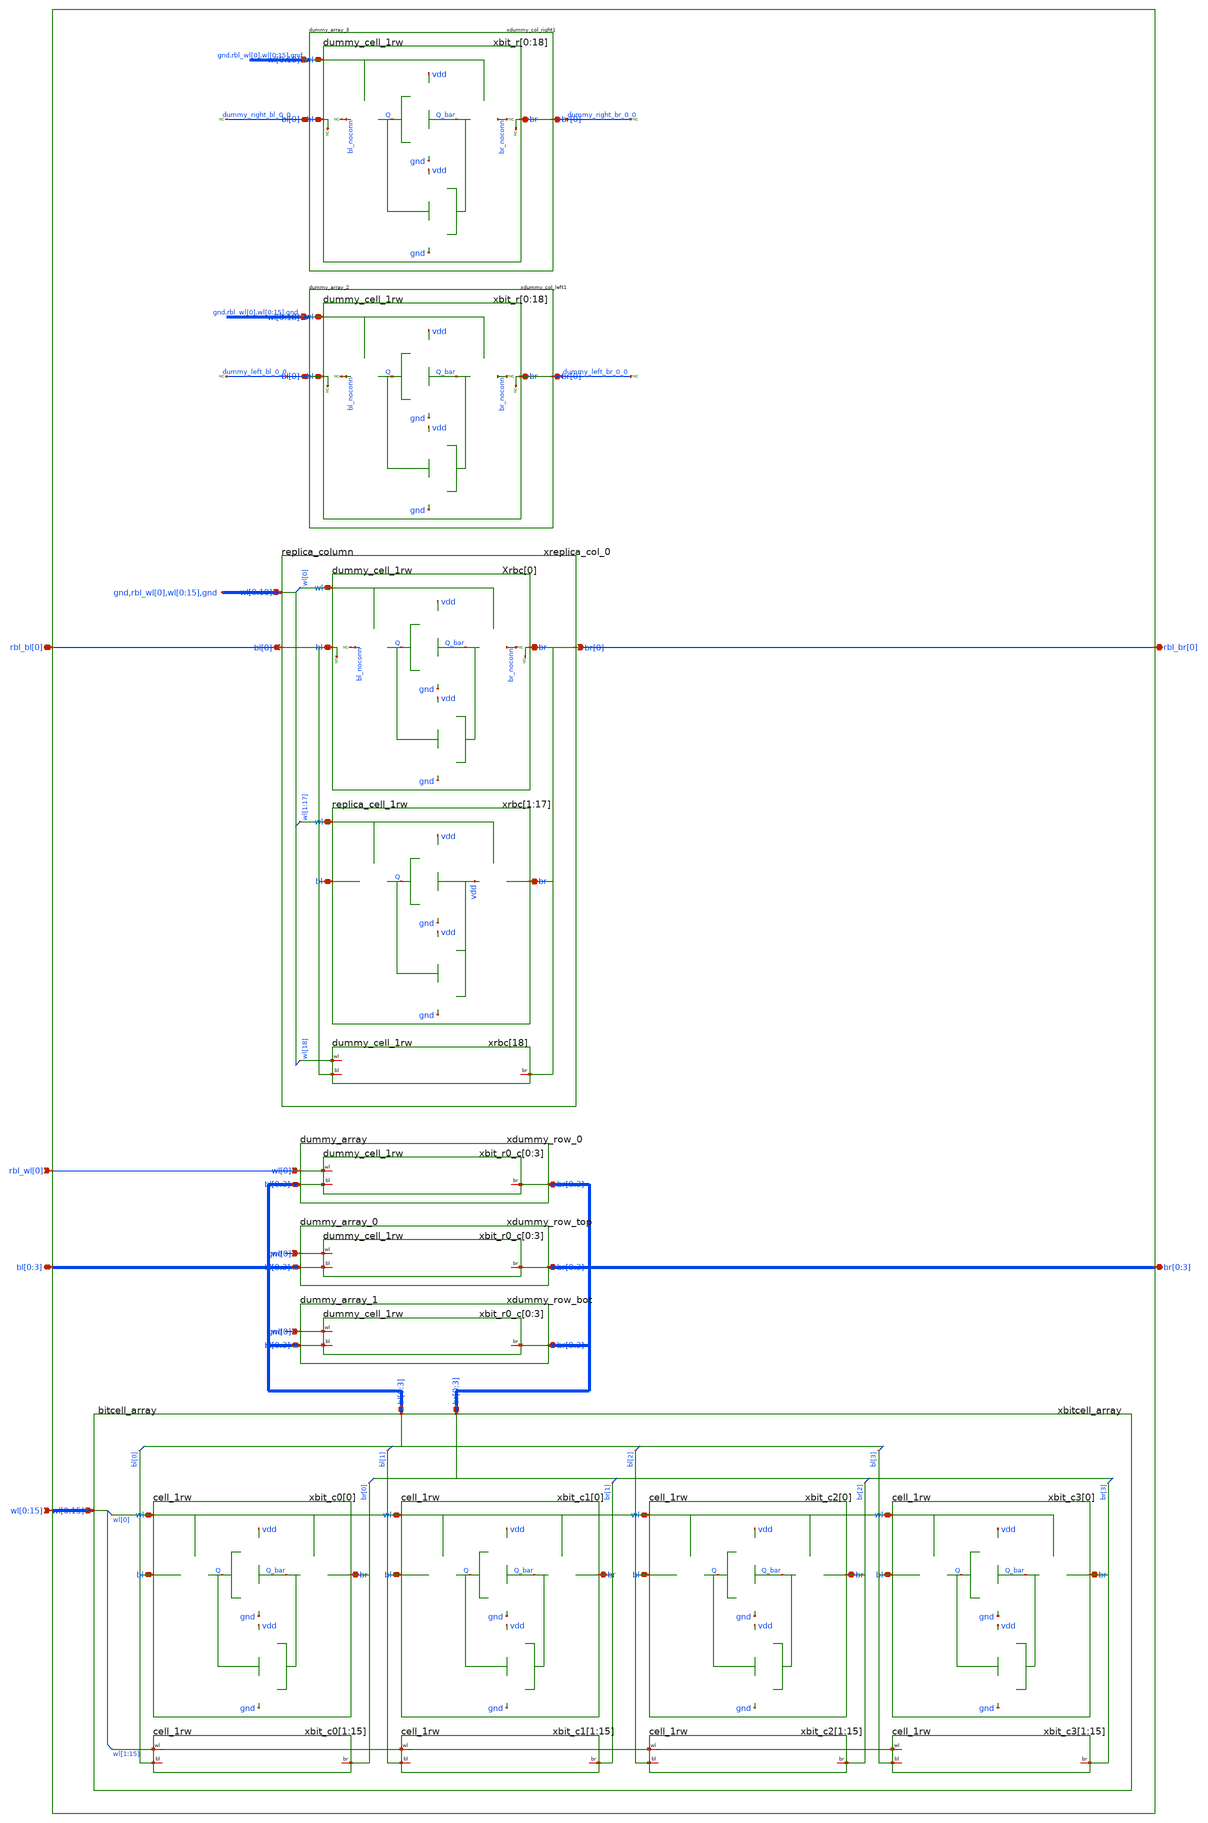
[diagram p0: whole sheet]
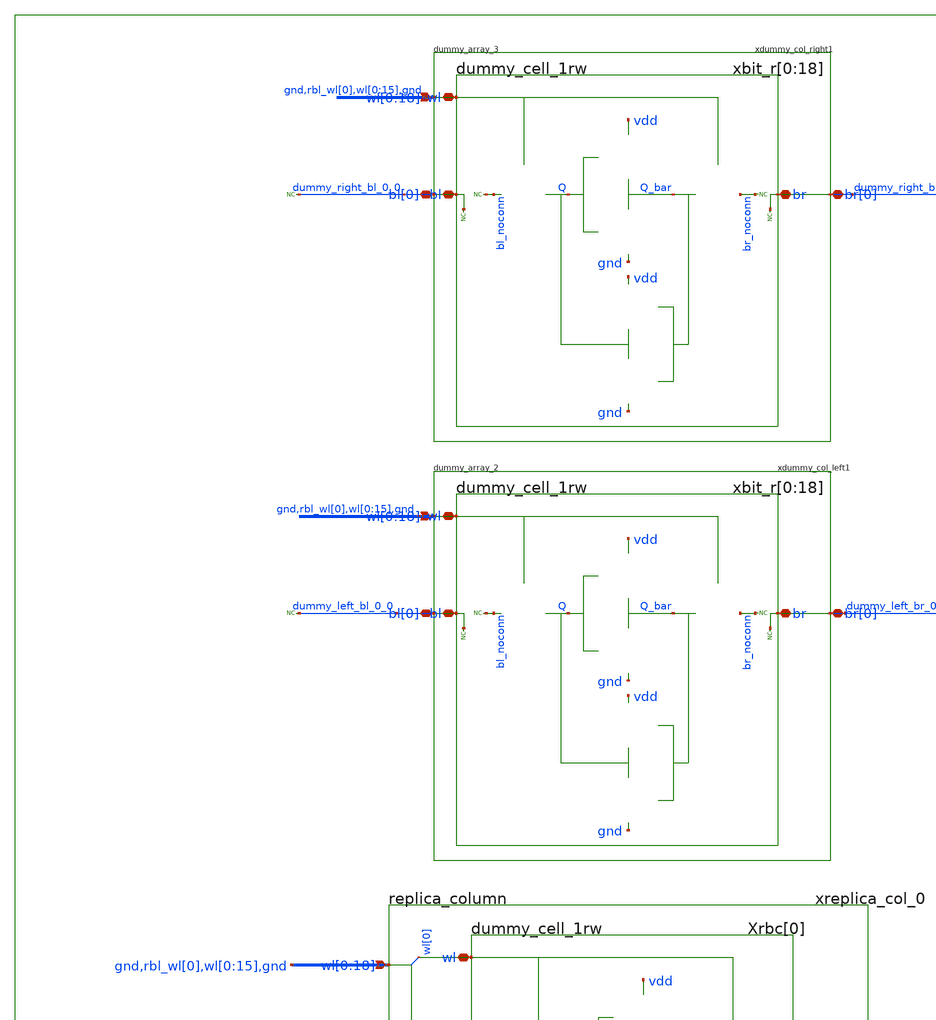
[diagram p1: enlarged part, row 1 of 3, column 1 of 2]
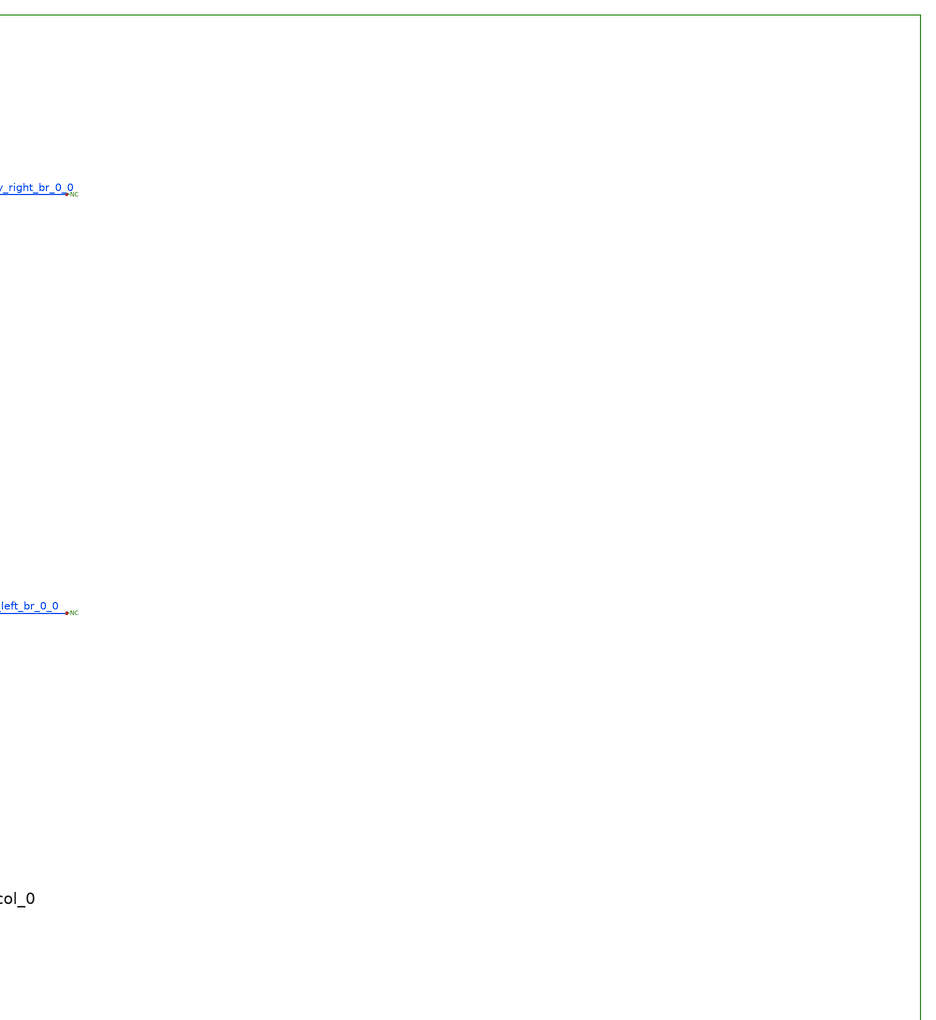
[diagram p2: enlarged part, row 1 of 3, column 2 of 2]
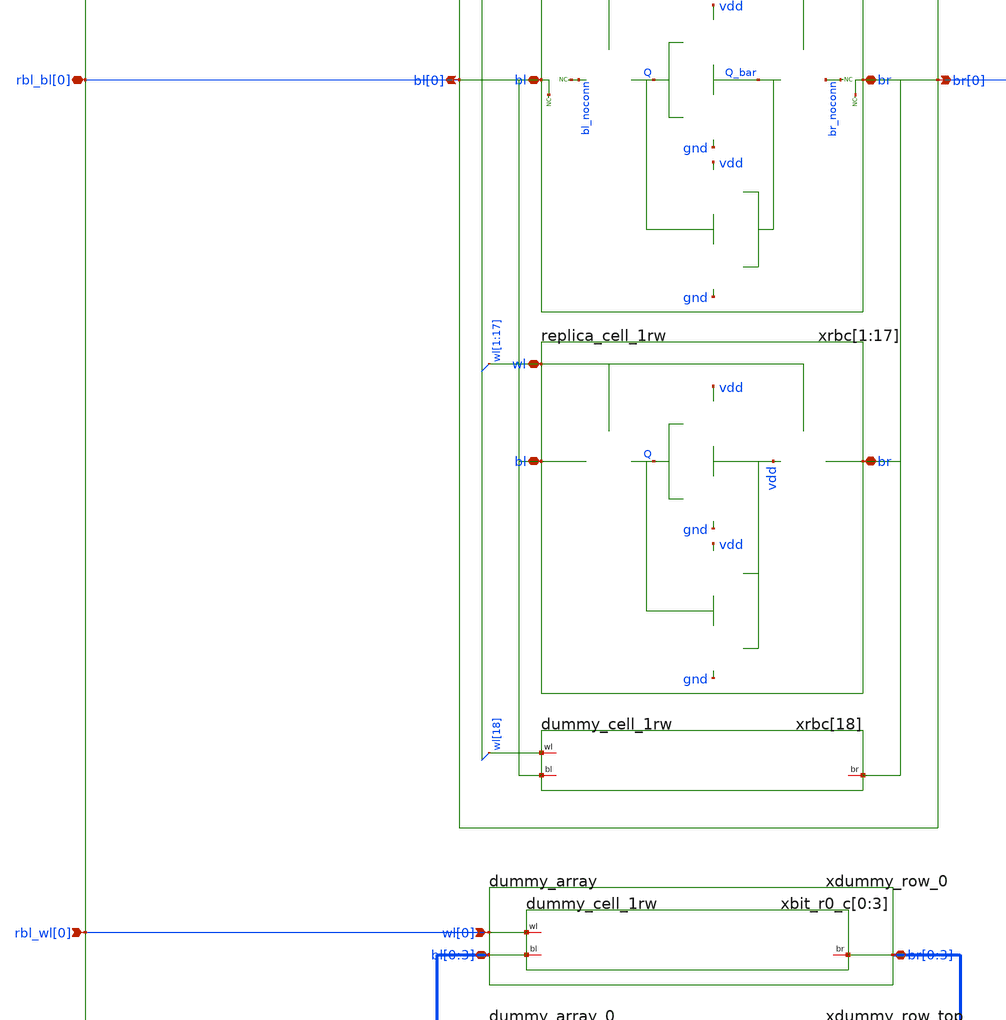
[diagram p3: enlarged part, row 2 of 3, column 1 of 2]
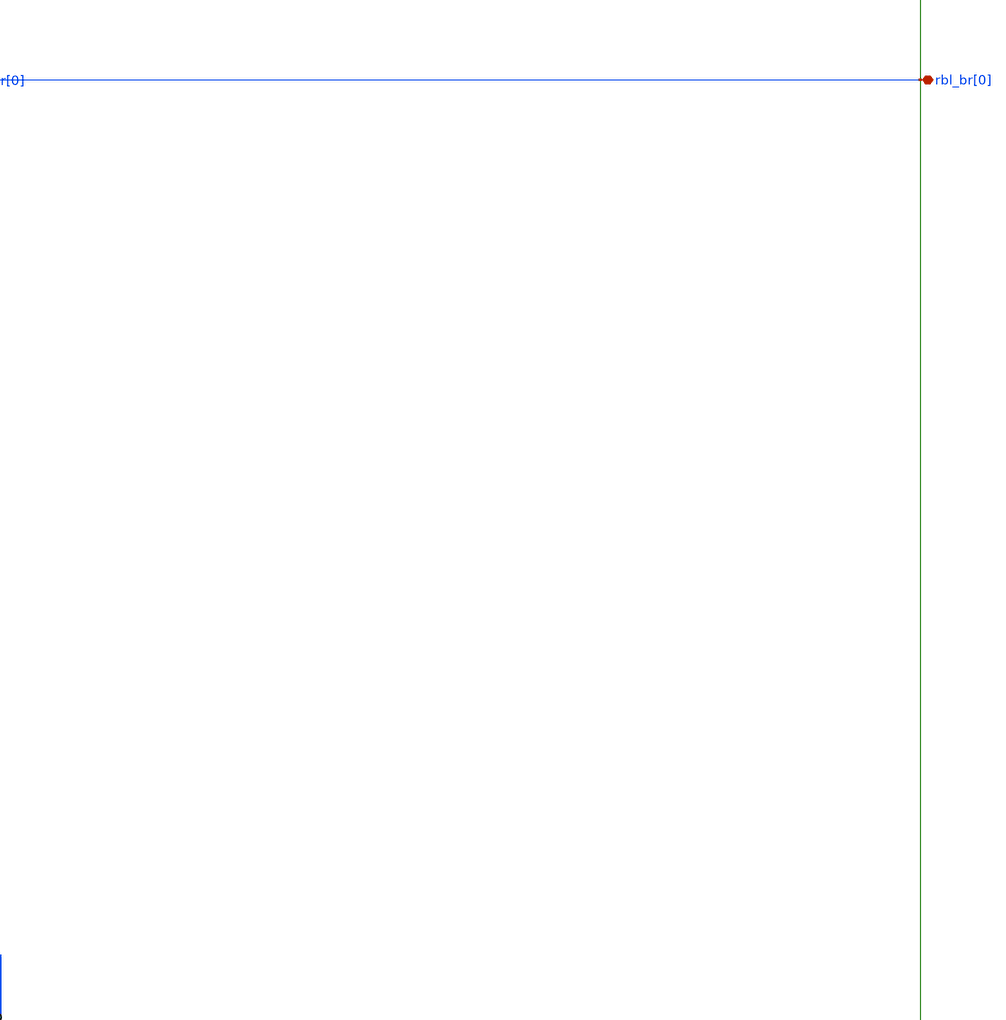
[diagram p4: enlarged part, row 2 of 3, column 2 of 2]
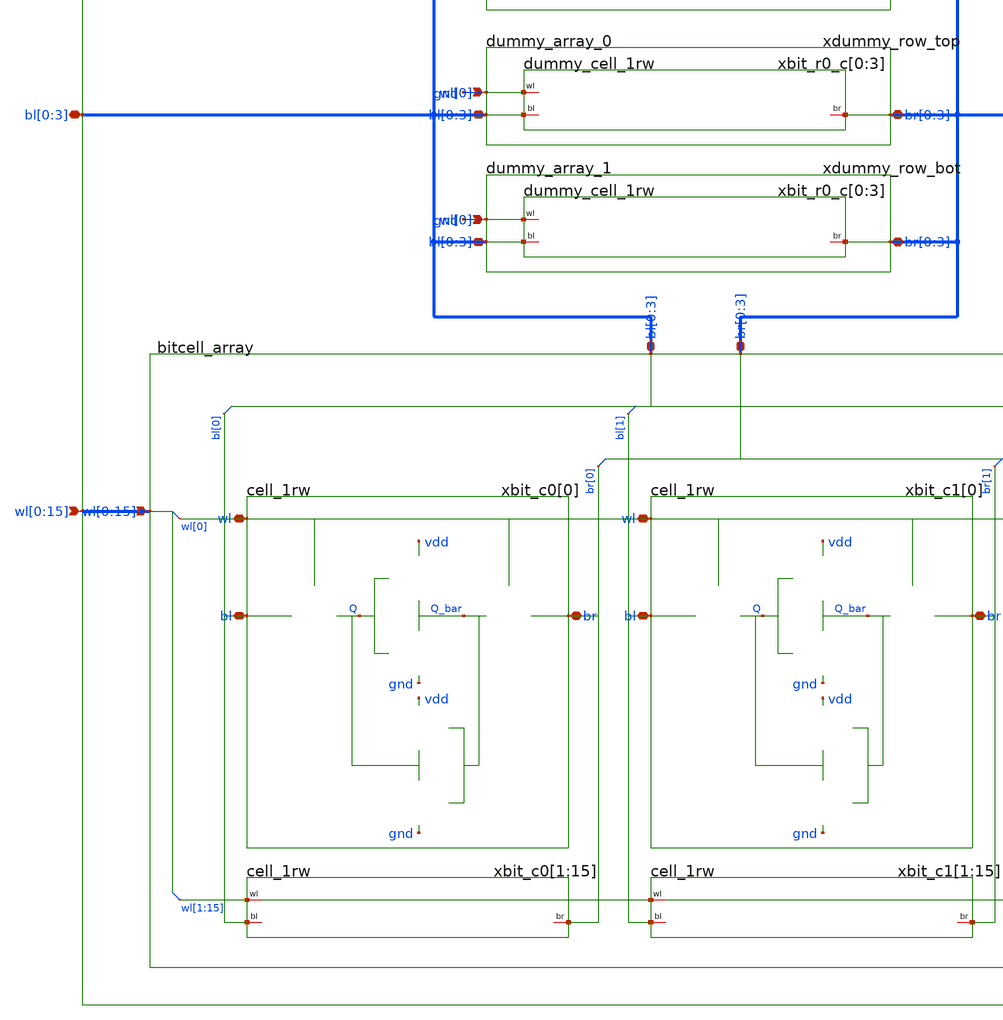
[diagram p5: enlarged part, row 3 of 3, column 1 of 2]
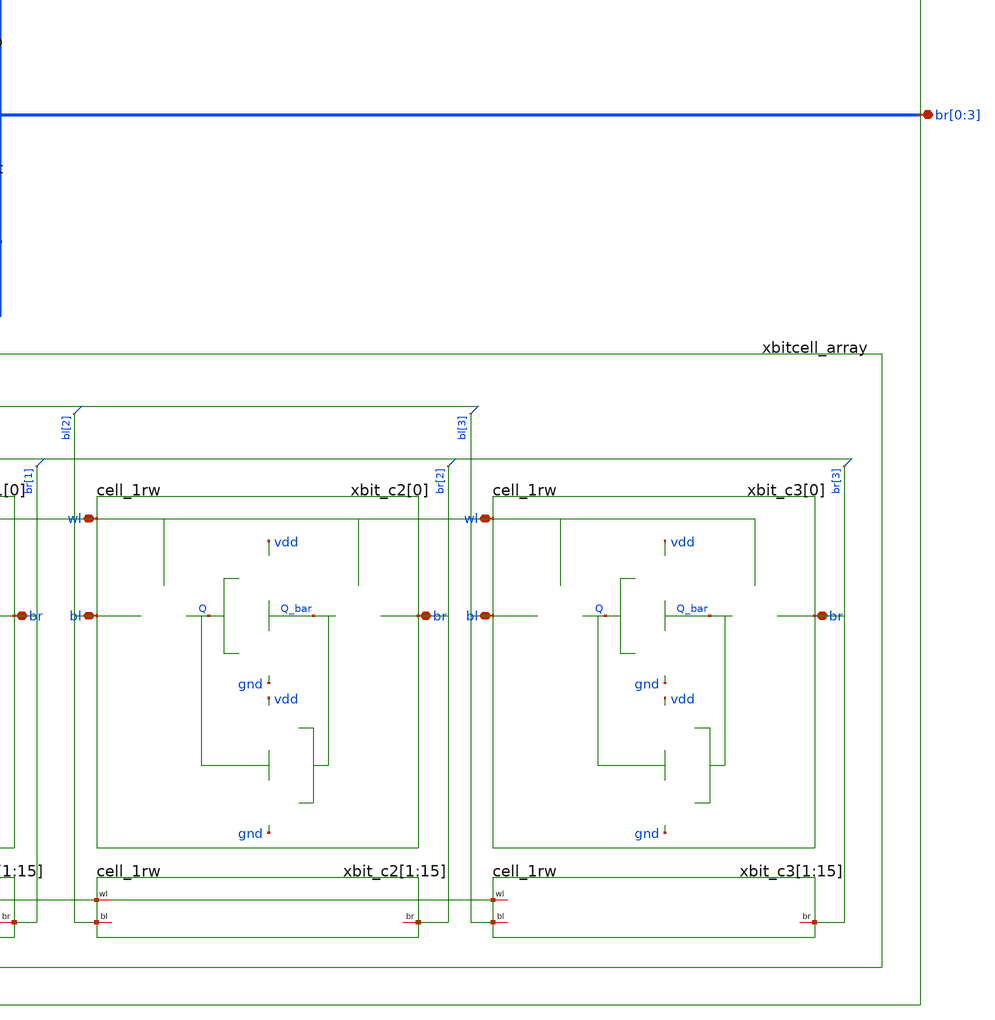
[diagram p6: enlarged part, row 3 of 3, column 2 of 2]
** sch_path: sram_4_16_scn4m/replica_bitcell_array.sch
**.subckt replica_bitcell_array rbl_bl[0] rbl_br[0] bl[0],bl[1],bl[2],bl[3] br[0],br[1],br[2],br[3]
*+ rbl_wl[0]
*+ wl[0],wl[1],wl[2],wl[3],wl[4],wl[5],wl[6],wl[7],wl[8],wl[9],wl[10],wl[11],wl[12],wl[13],wl[14],wl[15]
*.iopin rbl_bl[0]
*.iopin rbl_br[0]
*.iopin bl[0],bl[1],bl[2],bl[3]
*.iopin br[0],br[1],br[2],br[3]
*.ipin rbl_wl[0]
*.ipin
*+ wl[0],wl[1],wl[2],wl[3],wl[4],wl[5],wl[6],wl[7],wl[8],wl[9],wl[10],wl[11],wl[12],wl[13],wl[14],wl[15]
xbitcell_array bl[0] bl[1] bl[2] bl[3] br[0] br[1] br[2] br[3] wl[0] wl[1] wl[2] wl[3] wl[4] wl[5]
+ wl[6] wl[7] wl[8] wl[9] wl[10] wl[11] wl[12] wl[13] wl[14] wl[15] vdd gnd bitcell_array
xdummy_row_top bl[0] bl[1] bl[2] bl[3] br[0] br[1] br[2] br[3] gnd vdd gnd dummy_array_1
xdummy_row_0 bl[0] bl[1] bl[2] bl[3] br[0] br[1] br[2] br[3] rbl_wl[0] vdd gnd dummy_array
xdummy_col_left1 dummy_left_bl_0_0 dummy_left_br_0_0 gnd rbl_wl[0] wl[0] wl[1] wl[2] wl[3] wl[4]
+ wl[5] wl[6] wl[7] wl[8] wl[9] wl[10] wl[11] wl[12] wl[13] wl[14] wl[15] gnd vdd gnd dummy_array_2
xdummy_col_right1 dummy_right_bl_0_0 dummy_right_br_0_0 gnd rbl_wl[0] wl[0] wl[1] wl[2] wl[3] wl[4]
+ wl[5] wl[6] wl[7] wl[8] wl[9] wl[10] wl[11] wl[12] wl[13] wl[14] wl[15] gnd vdd gnd dummy_array_3
* noconn dummy_right_bl_0_0
* noconn dummy_right_br_0_0
* noconn dummy_left_bl_0_0
* noconn dummy_left_br_0_0
xdummy_row_bot bl[0] bl[1] bl[2] bl[3] br[0] br[1] br[2] br[3] gnd vdd gnd dummy_array_0
xreplica_col_0 rbl_bl[0] rbl_br[0] gnd rbl_wl[0] wl[0] wl[1] wl[2] wl[3] wl[4] wl[5] wl[6] wl[7]
+ wl[8] wl[9] wl[10] wl[11] wl[12] wl[13] wl[14] wl[15] gnd vdd gnd replica_column
**.ends

* expanding   symbol:  bitcell_array.sch # of pins=3
** sym_path: sram_4_16_scn4m/bitcell_array.sch
** sch_path: sram_4_16_scn4m/bitcell_array.sch
.subckt bitcell_array bl[0] bl[1] bl[2] bl[3] br[0] br[1] br[2] br[3] wl[0] wl[1] wl[2] wl[3] wl[4]
+ wl[5] wl[6] wl[7] wl[8] wl[9] wl[10] wl[11] wl[12] wl[13] wl[14] wl[15] vdd gnd
*.iopin bl[0],bl[1],bl[2],bl[3]
*.ipin
*+ wl[0],wl[1],wl[2],wl[3],wl[4],wl[5],wl[6],wl[7],wl[8],wl[9],wl[10],wl[11],wl[12],wl[13],wl[14],wl[15]
*.iopin br[0],br[1],br[2],br[3]
xbit_c0[1] bl[0] br[0] wl[1] vdd gnd cell_1rw
xbit_c0[2] bl[0] br[0] wl[2] vdd gnd cell_1rw
xbit_c0[3] bl[0] br[0] wl[3] vdd gnd cell_1rw
xbit_c0[4] bl[0] br[0] wl[4] vdd gnd cell_1rw
xbit_c0[5] bl[0] br[0] wl[5] vdd gnd cell_1rw
xbit_c0[6] bl[0] br[0] wl[6] vdd gnd cell_1rw
xbit_c0[7] bl[0] br[0] wl[7] vdd gnd cell_1rw
xbit_c0[8] bl[0] br[0] wl[8] vdd gnd cell_1rw
xbit_c0[9] bl[0] br[0] wl[9] vdd gnd cell_1rw
xbit_c0[10] bl[0] br[0] wl[10] vdd gnd cell_1rw
xbit_c0[11] bl[0] br[0] wl[11] vdd gnd cell_1rw
xbit_c0[12] bl[0] br[0] wl[12] vdd gnd cell_1rw
xbit_c0[13] bl[0] br[0] wl[13] vdd gnd cell_1rw
xbit_c0[14] bl[0] br[0] wl[14] vdd gnd cell_1rw
xbit_c0[15] bl[0] br[0] wl[15] vdd gnd cell_1rw
xbit_c0[0] bl[0] br[0] wl[0] vdd gnd cell_1rw
xbit_c1[1] bl[1] br[1] wl[1] vdd gnd cell_1rw
xbit_c1[2] bl[1] br[1] wl[2] vdd gnd cell_1rw
xbit_c1[3] bl[1] br[1] wl[3] vdd gnd cell_1rw
xbit_c1[4] bl[1] br[1] wl[4] vdd gnd cell_1rw
xbit_c1[5] bl[1] br[1] wl[5] vdd gnd cell_1rw
xbit_c1[6] bl[1] br[1] wl[6] vdd gnd cell_1rw
xbit_c1[7] bl[1] br[1] wl[7] vdd gnd cell_1rw
xbit_c1[8] bl[1] br[1] wl[8] vdd gnd cell_1rw
xbit_c1[9] bl[1] br[1] wl[9] vdd gnd cell_1rw
xbit_c1[10] bl[1] br[1] wl[10] vdd gnd cell_1rw
xbit_c1[11] bl[1] br[1] wl[11] vdd gnd cell_1rw
xbit_c1[12] bl[1] br[1] wl[12] vdd gnd cell_1rw
xbit_c1[13] bl[1] br[1] wl[13] vdd gnd cell_1rw
xbit_c1[14] bl[1] br[1] wl[14] vdd gnd cell_1rw
xbit_c1[15] bl[1] br[1] wl[15] vdd gnd cell_1rw
xbit_c1[0] bl[1] br[1] wl[0] vdd gnd cell_1rw
xbit_c2[1] bl[2] br[2] wl[1] vdd gnd cell_1rw
xbit_c2[2] bl[2] br[2] wl[2] vdd gnd cell_1rw
xbit_c2[3] bl[2] br[2] wl[3] vdd gnd cell_1rw
xbit_c2[4] bl[2] br[2] wl[4] vdd gnd cell_1rw
xbit_c2[5] bl[2] br[2] wl[5] vdd gnd cell_1rw
xbit_c2[6] bl[2] br[2] wl[6] vdd gnd cell_1rw
xbit_c2[7] bl[2] br[2] wl[7] vdd gnd cell_1rw
xbit_c2[8] bl[2] br[2] wl[8] vdd gnd cell_1rw
xbit_c2[9] bl[2] br[2] wl[9] vdd gnd cell_1rw
xbit_c2[10] bl[2] br[2] wl[10] vdd gnd cell_1rw
xbit_c2[11] bl[2] br[2] wl[11] vdd gnd cell_1rw
xbit_c2[12] bl[2] br[2] wl[12] vdd gnd cell_1rw
xbit_c2[13] bl[2] br[2] wl[13] vdd gnd cell_1rw
xbit_c2[14] bl[2] br[2] wl[14] vdd gnd cell_1rw
xbit_c2[15] bl[2] br[2] wl[15] vdd gnd cell_1rw
xbit_c2[0] bl[2] br[2] wl[0] vdd gnd cell_1rw
xbit_c3[1] bl[3] br[3] wl[1] vdd gnd cell_1rw
xbit_c3[2] bl[3] br[3] wl[2] vdd gnd cell_1rw
xbit_c3[3] bl[3] br[3] wl[3] vdd gnd cell_1rw
xbit_c3[4] bl[3] br[3] wl[4] vdd gnd cell_1rw
xbit_c3[5] bl[3] br[3] wl[5] vdd gnd cell_1rw
xbit_c3[6] bl[3] br[3] wl[6] vdd gnd cell_1rw
xbit_c3[7] bl[3] br[3] wl[7] vdd gnd cell_1rw
xbit_c3[8] bl[3] br[3] wl[8] vdd gnd cell_1rw
xbit_c3[9] bl[3] br[3] wl[9] vdd gnd cell_1rw
xbit_c3[10] bl[3] br[3] wl[10] vdd gnd cell_1rw
xbit_c3[11] bl[3] br[3] wl[11] vdd gnd cell_1rw
xbit_c3[12] bl[3] br[3] wl[12] vdd gnd cell_1rw
xbit_c3[13] bl[3] br[3] wl[13] vdd gnd cell_1rw
xbit_c3[14] bl[3] br[3] wl[14] vdd gnd cell_1rw
xbit_c3[15] bl[3] br[3] wl[15] vdd gnd cell_1rw
xbit_c3[0] bl[3] br[3] wl[0] vdd gnd cell_1rw
.ends


* expanding   symbol:  dummy_array_0.sch # of pins=3
** sym_path: sram_4_16_scn4m/dummy_array_0.sch
** sch_path: sram_4_16_scn4m/dummy_array_0.sch
.subckt dummy_array_0 bl[0] bl[1] bl[2] bl[3] br[0] br[1] br[2] br[3] wl[0] vdd gnd
*.iopin bl[0],bl[1],bl[2],bl[3]
*.iopin br[0],br[1],br[2],br[3]
*.ipin wl[0]
xbit_r0_c[0] bl[0] br[0] wl[0] vdd gnd dummy_cell_1rw
xbit_r0_c[1] bl[1] br[1] wl[0] vdd gnd dummy_cell_1rw
xbit_r0_c[2] bl[2] br[2] wl[0] vdd gnd dummy_cell_1rw
xbit_r0_c[3] bl[3] br[3] wl[0] vdd gnd dummy_cell_1rw
.ends


* expanding   symbol:  dummy_array.sch # of pins=3
** sym_path: sram_4_16_scn4m/dummy_array.sch
** sch_path: sram_4_16_scn4m/dummy_array.sch
.subckt dummy_array bl[0] bl[1] bl[2] bl[3] br[0] br[1] br[2] br[3] wl[0] vdd gnd
*.iopin bl[0],bl[1],bl[2],bl[3]
*.iopin br[0],br[1],br[2],br[3]
*.ipin wl[0]
xbit_r0_c[0] bl[0] br[0] wl[0] vdd gnd dummy_cell_1rw
xbit_r0_c[1] bl[1] br[1] wl[0] vdd gnd dummy_cell_1rw
xbit_r0_c[2] bl[2] br[2] wl[0] vdd gnd dummy_cell_1rw
xbit_r0_c[3] bl[3] br[3] wl[0] vdd gnd dummy_cell_1rw
.ends


* expanding   symbol:  dummy_array_2.sch # of pins=3
** sym_path: sram_4_16_scn4m/dummy_array_2.sch
** sch_path: sram_4_16_scn4m/dummy_array_2.sch
.subckt dummy_array_2 bl[0] br[0] wl[0] wl[1] wl[2] wl[3] wl[4] wl[5] wl[6] wl[7] wl[8] wl[9] wl[10]
+ wl[11] wl[12] wl[13] wl[14] wl[15] wl[16] wl[17] wl[18] vdd gnd
*.iopin bl[0]
*.iopin br[0]
*.ipin
*+ wl[0],wl[1],wl[2],wl[3],wl[4],wl[5],wl[6],wl[7],wl[8],wl[9],wl[10],wl[11],wl[12],wl[13],wl[14],wl[15],wl[16],wl[17],wl[18]
xbit_r[0] bl[0] br[0] wl[0] vdd gnd dummy_cell_1rw
xbit_r[1] bl[0] br[0] wl[1] vdd gnd dummy_cell_1rw
xbit_r[2] bl[0] br[0] wl[2] vdd gnd dummy_cell_1rw
xbit_r[3] bl[0] br[0] wl[3] vdd gnd dummy_cell_1rw
xbit_r[4] bl[0] br[0] wl[4] vdd gnd dummy_cell_1rw
xbit_r[5] bl[0] br[0] wl[5] vdd gnd dummy_cell_1rw
xbit_r[6] bl[0] br[0] wl[6] vdd gnd dummy_cell_1rw
xbit_r[7] bl[0] br[0] wl[7] vdd gnd dummy_cell_1rw
xbit_r[8] bl[0] br[0] wl[8] vdd gnd dummy_cell_1rw
xbit_r[9] bl[0] br[0] wl[9] vdd gnd dummy_cell_1rw
xbit_r[10] bl[0] br[0] wl[10] vdd gnd dummy_cell_1rw
xbit_r[11] bl[0] br[0] wl[11] vdd gnd dummy_cell_1rw
xbit_r[12] bl[0] br[0] wl[12] vdd gnd dummy_cell_1rw
xbit_r[13] bl[0] br[0] wl[13] vdd gnd dummy_cell_1rw
xbit_r[14] bl[0] br[0] wl[14] vdd gnd dummy_cell_1rw
xbit_r[15] bl[0] br[0] wl[15] vdd gnd dummy_cell_1rw
xbit_r[16] bl[0] br[0] wl[16] vdd gnd dummy_cell_1rw
xbit_r[17] bl[0] br[0] wl[17] vdd gnd dummy_cell_1rw
xbit_r[18] bl[0] br[0] wl[18] vdd gnd dummy_cell_1rw
.ends


* expanding   symbol:  dummy_array_3.sch # of pins=3
** sym_path: sram_4_16_scn4m/dummy_array_3.sch
** sch_path: sram_4_16_scn4m/dummy_array_3.sch
.subckt dummy_array_3 bl[0] br[0] wl[0] wl[1] wl[2] wl[3] wl[4] wl[5] wl[6] wl[7] wl[8] wl[9] wl[10]
+ wl[11] wl[12] wl[13] wl[14] wl[15] wl[16] wl[17] wl[18] vdd gnd
*.iopin br[0]
*.iopin bl[0]
*.ipin
*+ wl[0],wl[1],wl[2],wl[3],wl[4],wl[5],wl[6],wl[7],wl[8],wl[9],wl[10],wl[11],wl[12],wl[13],wl[14],wl[15],wl[16],wl[17],wl[18]
xbit_r[0] bl[0] br[0] wl[0] vdd gnd dummy_cell_1rw
xbit_r[1] bl[0] br[0] wl[1] vdd gnd dummy_cell_1rw
xbit_r[2] bl[0] br[0] wl[2] vdd gnd dummy_cell_1rw
xbit_r[3] bl[0] br[0] wl[3] vdd gnd dummy_cell_1rw
xbit_r[4] bl[0] br[0] wl[4] vdd gnd dummy_cell_1rw
xbit_r[5] bl[0] br[0] wl[5] vdd gnd dummy_cell_1rw
xbit_r[6] bl[0] br[0] wl[6] vdd gnd dummy_cell_1rw
xbit_r[7] bl[0] br[0] wl[7] vdd gnd dummy_cell_1rw
xbit_r[8] bl[0] br[0] wl[8] vdd gnd dummy_cell_1rw
xbit_r[9] bl[0] br[0] wl[9] vdd gnd dummy_cell_1rw
xbit_r[10] bl[0] br[0] wl[10] vdd gnd dummy_cell_1rw
xbit_r[11] bl[0] br[0] wl[11] vdd gnd dummy_cell_1rw
xbit_r[12] bl[0] br[0] wl[12] vdd gnd dummy_cell_1rw
xbit_r[13] bl[0] br[0] wl[13] vdd gnd dummy_cell_1rw
xbit_r[14] bl[0] br[0] wl[14] vdd gnd dummy_cell_1rw
xbit_r[15] bl[0] br[0] wl[15] vdd gnd dummy_cell_1rw
xbit_r[16] bl[0] br[0] wl[16] vdd gnd dummy_cell_1rw
xbit_r[17] bl[0] br[0] wl[17] vdd gnd dummy_cell_1rw
xbit_r[18] bl[0] br[0] wl[18] vdd gnd dummy_cell_1rw
.ends


* expanding   symbol:  dummy_array_1.sch # of pins=3
** sym_path: sram_4_16_scn4m/dummy_array_1.sch
** sch_path: sram_4_16_scn4m/dummy_array_1.sch
.subckt dummy_array_1 bl[0] bl[1] bl[2] bl[3] br[0] br[1] br[2] br[3] wl[0] vdd gnd
*.iopin bl[0],bl[1],bl[2],bl[3]
*.iopin br[0],br[1],br[2],br[3]
*.ipin wl[0]
xbit_r0_c[0] bl[0] br[0] wl[0] vdd gnd dummy_cell_1rw
xbit_r0_c[1] bl[1] br[1] wl[0] vdd gnd dummy_cell_1rw
xbit_r0_c[2] bl[2] br[2] wl[0] vdd gnd dummy_cell_1rw
xbit_r0_c[3] bl[3] br[3] wl[0] vdd gnd dummy_cell_1rw
.ends


* expanding   symbol:  replica_column.sch # of pins=3
** sym_path: sram_4_16_scn4m/replica_column.sch
** sch_path: sram_4_16_scn4m/replica_column.sch
.subckt replica_column bl[0] br[0] wl[0] wl[1] wl[2] wl[3] wl[4] wl[5] wl[6] wl[7] wl[8] wl[9]
+ wl[10] wl[11] wl[12] wl[13] wl[14] wl[15] wl[16] wl[17] wl[18] vdd gnd
*.opin bl[0]
*.opin br[0]
*.ipin
*+ wl[0],wl[1],wl[2],wl[3],wl[4],wl[5],wl[6],wl[7],wl[8],wl[9],wl[10],wl[11],wl[12],wl[13],wl[14],wl[15],wl[16],wl[17],wl[18]
Xrbc[0] bl[0] br[0] wl[0] vdd gnd dummy_cell_1rw
xrbc[1] bl[0] br[0] wl[1] vdd gnd replica_cell_1rw
xrbc[2] bl[0] br[0] wl[2] vdd gnd replica_cell_1rw
xrbc[3] bl[0] br[0] wl[3] vdd gnd replica_cell_1rw
xrbc[4] bl[0] br[0] wl[4] vdd gnd replica_cell_1rw
xrbc[5] bl[0] br[0] wl[5] vdd gnd replica_cell_1rw
xrbc[6] bl[0] br[0] wl[6] vdd gnd replica_cell_1rw
xrbc[7] bl[0] br[0] wl[7] vdd gnd replica_cell_1rw
xrbc[8] bl[0] br[0] wl[8] vdd gnd replica_cell_1rw
xrbc[9] bl[0] br[0] wl[9] vdd gnd replica_cell_1rw
xrbc[10] bl[0] br[0] wl[10] vdd gnd replica_cell_1rw
xrbc[11] bl[0] br[0] wl[11] vdd gnd replica_cell_1rw
xrbc[12] bl[0] br[0] wl[12] vdd gnd replica_cell_1rw
xrbc[13] bl[0] br[0] wl[13] vdd gnd replica_cell_1rw
xrbc[14] bl[0] br[0] wl[14] vdd gnd replica_cell_1rw
xrbc[15] bl[0] br[0] wl[15] vdd gnd replica_cell_1rw
xrbc[16] bl[0] br[0] wl[16] vdd gnd replica_cell_1rw
xrbc[17] bl[0] br[0] wl[17] vdd gnd replica_cell_1rw
xrbc[18] bl[0] br[0] wl[18] vdd gnd dummy_cell_1rw
.ends


* expanding   symbol:  cell_1rw.sym # of pins=3
** sym_path: sram_4_16_scn4m/cell_1rw.sym
** sch_path: sram_4_16_scn4m/cell_1rw.sch
.subckt cell_1rw bl br wl vdd gnd
*.iopin bl
*.iopin br
*.iopin wl
XM1004 Q wl bl gnd sky130_fd_pr__nfet_01v8 L=0.4 W=0.8 nf=1 ad='int((nf+1)/2) * W/nf * 0.29' as='int((nf+2)/2) * W/nf * 0.29'
+ pd='2*int((nf+1)/2) * (W/nf + 0.29)' ps='2*int((nf+2)/2) * (W/nf + 0.29)' nrd='0.29 / W' nrs='0.29 / W'
+ sa=0 sb=0 sd=0 mult=1 m=1
XM1001 Q_bar Q vdd vdd sky130_fd_pr__pfet_01v8 L=0.8 W=0.6 nf=1 ad='int((nf+1)/2) * W/nf * 0.29' as='int((nf+2)/2) * W/nf * 0.29'
+ pd='2*int((nf+1)/2) * (W/nf + 0.29)' ps='2*int((nf+2)/2) * (W/nf + 0.29)' nrd='0.29 / W' nrs='0.29 / W'
+ sa=0 sb=0 sd=0 mult=1 m=1
XM1003 Q_bar Q gnd gnd sky130_fd_pr__nfet_01v8 L=0.4 W=1.6 nf=1 ad='int((nf+1)/2) * W/nf * 0.29' as='int((nf+2)/2) * W/nf * 0.29'
+ pd='2*int((nf+1)/2) * (W/nf + 0.29)' ps='2*int((nf+2)/2) * (W/nf + 0.29)' nrd='0.29 / W' nrs='0.29 / W'
+ sa=0 sb=0 sd=0 mult=1 m=1
XM1002 Q Q_bar gnd gnd sky130_fd_pr__nfet_01v8 L=0.4 W=1.6 nf=1 ad='int((nf+1)/2) * W/nf * 0.29' as='int((nf+2)/2) * W/nf * 0.29'
+ pd='2*int((nf+1)/2) * (W/nf + 0.29)' ps='2*int((nf+2)/2) * (W/nf + 0.29)' nrd='0.29 / W' nrs='0.29 / W'
+ sa=0 sb=0 sd=0 mult=1 m=1
XM1000 Q Q_bar vdd vdd sky130_fd_pr__pfet_01v8 L=0.8 W=0.6 nf=1 ad='int((nf+1)/2) * W/nf * 0.29' as='int((nf+2)/2) * W/nf * 0.29'
+ pd='2*int((nf+1)/2) * (W/nf + 0.29)' ps='2*int((nf+2)/2) * (W/nf + 0.29)' nrd='0.29 / W' nrs='0.29 / W'
+ sa=0 sb=0 sd=0 mult=1 m=1
XM1005 br wl Q_bar gnd sky130_fd_pr__nfet_01v8 L=0.4 W=0.8 nf=1 ad='int((nf+1)/2) * W/nf * 0.29' as='int((nf+2)/2) * W/nf * 0.29'
+ pd='2*int((nf+1)/2) * (W/nf + 0.29)' ps='2*int((nf+2)/2) * (W/nf + 0.29)' nrd='0.29 / W' nrs='0.29 / W'
+ sa=0 sb=0 sd=0 mult=1 m=1
.ends


* expanding   symbol:  dummy_cell_1rw.sym # of pins=3
** sym_path: sram_4_16_scn4m/dummy_cell_1rw.sym
** sch_path: sram_4_16_scn4m/dummy_cell_1rw.sch
.subckt dummy_cell_1rw bl br wl vdd gnd
*.iopin bl
*.iopin br
*.iopin wl
XM1004 Q wl bl_noconn gnd sky130_fd_pr__nfet_01v8 L=0.4 W=0.8 nf=1 ad='int((nf+1)/2) * W/nf * 0.29' as='int((nf+2)/2) * W/nf * 0.29'
+ pd='2*int((nf+1)/2) * (W/nf + 0.29)' ps='2*int((nf+2)/2) * (W/nf + 0.29)' nrd='0.29 / W' nrs='0.29 / W'
+ sa=0 sb=0 sd=0 mult=1 m=1
XM1001 Q_bar Q vdd vdd sky130_fd_pr__pfet_01v8 L=0.8 W=0.6 nf=1 ad='int((nf+1)/2) * W/nf * 0.29' as='int((nf+2)/2) * W/nf * 0.29'
+ pd='2*int((nf+1)/2) * (W/nf + 0.29)' ps='2*int((nf+2)/2) * (W/nf + 0.29)' nrd='0.29 / W' nrs='0.29 / W'
+ sa=0 sb=0 sd=0 mult=1 m=1
XM1003 Q_bar Q gnd gnd sky130_fd_pr__nfet_01v8 L=0.4 W=1.6 nf=1 ad='int((nf+1)/2) * W/nf * 0.29' as='int((nf+2)/2) * W/nf * 0.29'
+ pd='2*int((nf+1)/2) * (W/nf + 0.29)' ps='2*int((nf+2)/2) * (W/nf + 0.29)' nrd='0.29 / W' nrs='0.29 / W'
+ sa=0 sb=0 sd=0 mult=1 m=1
XM1002 Q Q_bar gnd gnd sky130_fd_pr__nfet_01v8 L=0.4 W=1.6 nf=1 ad='int((nf+1)/2) * W/nf * 0.29' as='int((nf+2)/2) * W/nf * 0.29'
+ pd='2*int((nf+1)/2) * (W/nf + 0.29)' ps='2*int((nf+2)/2) * (W/nf + 0.29)' nrd='0.29 / W' nrs='0.29 / W'
+ sa=0 sb=0 sd=0 mult=1 m=1
XM1000 Q Q_bar vdd vdd sky130_fd_pr__pfet_01v8 L=0.8 W=0.6 nf=1 ad='int((nf+1)/2) * W/nf * 0.29' as='int((nf+2)/2) * W/nf * 0.29'
+ pd='2*int((nf+1)/2) * (W/nf + 0.29)' ps='2*int((nf+2)/2) * (W/nf + 0.29)' nrd='0.29 / W' nrs='0.29 / W'
+ sa=0 sb=0 sd=0 mult=1 m=1
XM1005 br_noconn wl Q_bar gnd sky130_fd_pr__nfet_01v8 L=0.4 W=0.8 nf=1 ad='int((nf+1)/2) * W/nf * 0.29'
+ as='int((nf+2)/2) * W/nf * 0.29' pd='2*int((nf+1)/2) * (W/nf + 0.29)' ps='2*int((nf+2)/2) * (W/nf + 0.29)'
+ nrd='0.29 / W' nrs='0.29 / W' sa=0 sb=0 sd=0 mult=1 m=1
* noconn bl_noconn
* noconn br_noconn
* noconn br
* noconn bl
.ends


* expanding   symbol:  replica_cell_1rw.sch # of pins=3
** sym_path: sram_4_16_scn4m/replica_cell_1rw.sch
** sch_path: sram_4_16_scn4m/replica_cell_1rw.sch
.subckt replica_cell_1rw bl br wl vdd gnd
*.iopin bl
*.iopin br
*.iopin wl
XM1004 Q wl bl gnd sky130_fd_pr__nfet_01v8 L=0.4 W=0.8 nf=1 ad='int((nf+1)/2) * W/nf * 0.29' as='int((nf+2)/2) * W/nf * 0.29'
+ pd='2*int((nf+1)/2) * (W/nf + 0.29)' ps='2*int((nf+2)/2) * (W/nf + 0.29)' nrd='0.29 / W' nrs='0.29 / W'
+ sa=0 sb=0 sd=0 mult=1 m=1
XM1001 vdd Q vdd vdd sky130_fd_pr__pfet_01v8 L=0.8 W=0.6 nf=1 ad='int((nf+1)/2) * W/nf * 0.29' as='int((nf+2)/2) * W/nf * 0.29'
+ pd='2*int((nf+1)/2) * (W/nf + 0.29)' ps='2*int((nf+2)/2) * (W/nf + 0.29)' nrd='0.29 / W' nrs='0.29 / W'
+ sa=0 sb=0 sd=0 mult=1 m=1
XM1003 vdd Q gnd gnd sky130_fd_pr__nfet_01v8 L=0.4 W=1.6 nf=1 ad='int((nf+1)/2) * W/nf * 0.29' as='int((nf+2)/2) * W/nf * 0.29'
+ pd='2*int((nf+1)/2) * (W/nf + 0.29)' ps='2*int((nf+2)/2) * (W/nf + 0.29)' nrd='0.29 / W' nrs='0.29 / W'
+ sa=0 sb=0 sd=0 mult=1 m=1
XM1002 Q vdd gnd gnd sky130_fd_pr__nfet_01v8 L=0.4 W=1.6 nf=1 ad='int((nf+1)/2) * W/nf * 0.29' as='int((nf+2)/2) * W/nf * 0.29'
+ pd='2*int((nf+1)/2) * (W/nf + 0.29)' ps='2*int((nf+2)/2) * (W/nf + 0.29)' nrd='0.29 / W' nrs='0.29 / W'
+ sa=0 sb=0 sd=0 mult=1 m=1
XM1000 Q vdd vdd vdd sky130_fd_pr__pfet_01v8 L=0.8 W=0.6 nf=1 ad='int((nf+1)/2) * W/nf * 0.29' as='int((nf+2)/2) * W/nf * 0.29'
+ pd='2*int((nf+1)/2) * (W/nf + 0.29)' ps='2*int((nf+2)/2) * (W/nf + 0.29)' nrd='0.29 / W' nrs='0.29 / W'
+ sa=0 sb=0 sd=0 mult=1 m=1
XM1005 br wl vdd gnd sky130_fd_pr__nfet_01v8 L=0.4 W=0.8 nf=1 ad='int((nf+1)/2) * W/nf * 0.29' as='int((nf+2)/2) * W/nf * 0.29'
+ pd='2*int((nf+1)/2) * (W/nf + 0.29)' ps='2*int((nf+2)/2) * (W/nf + 0.29)' nrd='0.29 / W' nrs='0.29 / W'
+ sa=0 sb=0 sd=0 mult=1 m=1
.ends

.end
